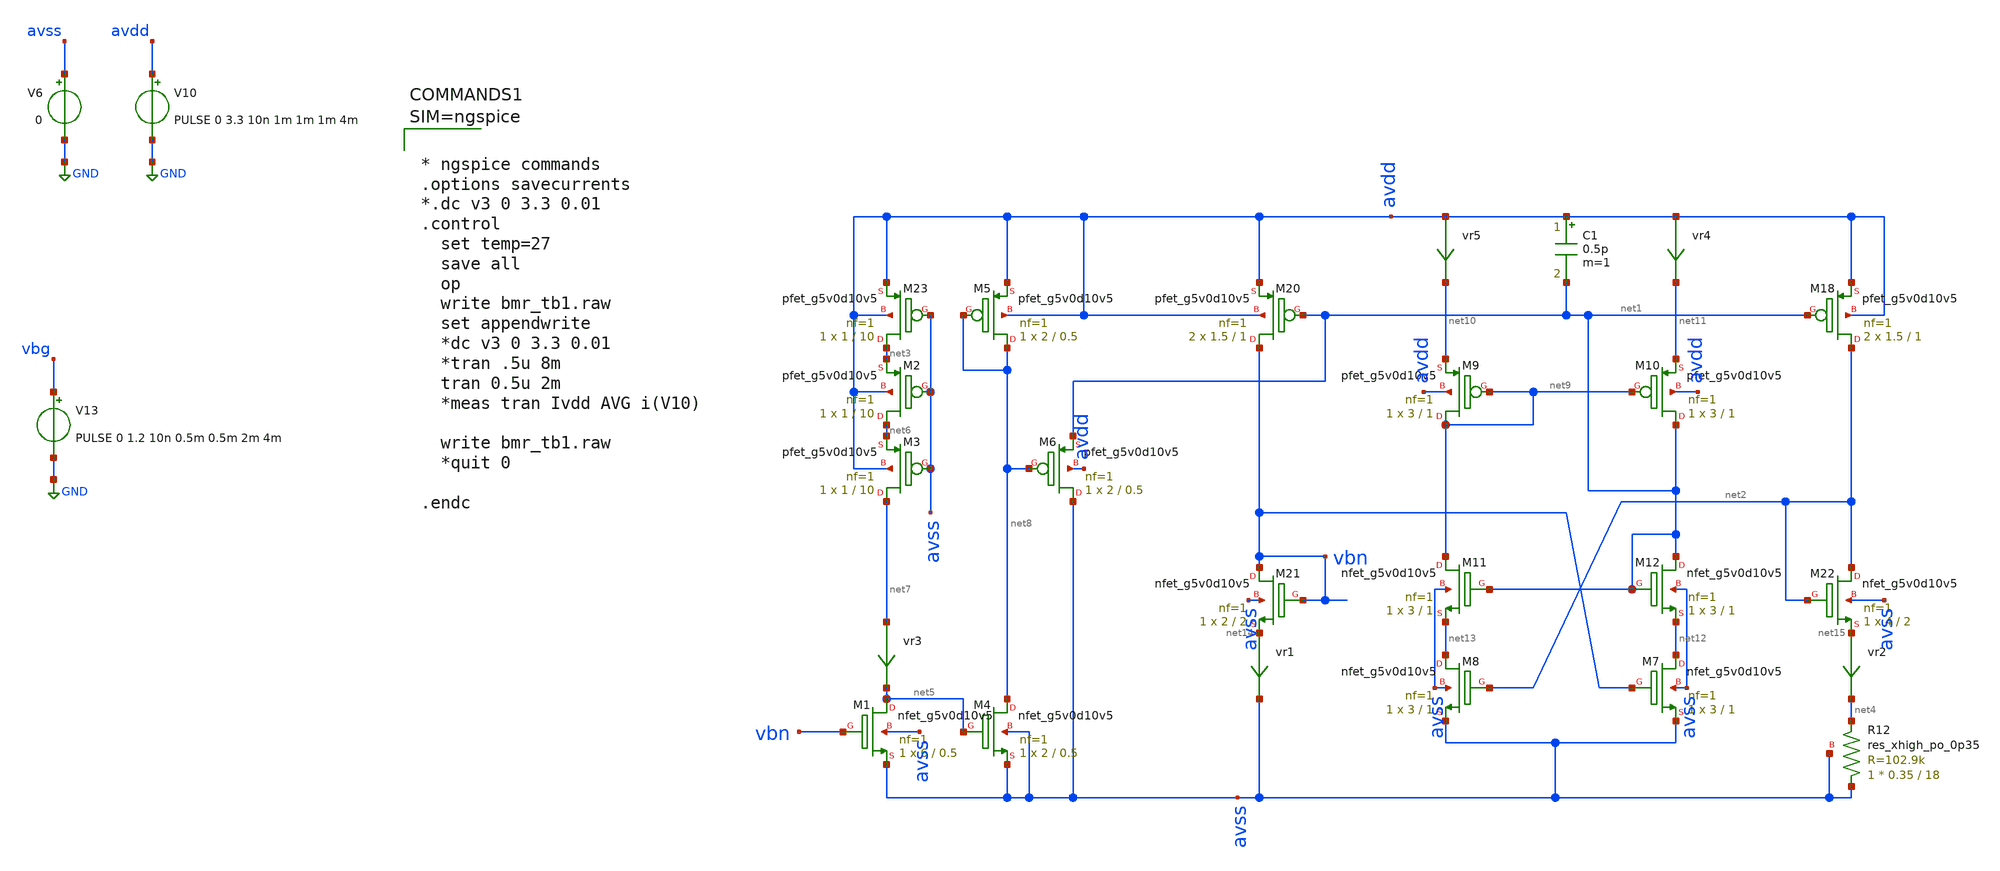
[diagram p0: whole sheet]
** sch_path: xschem_sim/bmr_tb1.sch
**.subckt bmr_tb1
XM18 net2 net1 avdd avdd sky130_fd_pr__pfet_g5v0d10v5 L=1 W=1.5 nf=1 ad='int((nf+1)/2) * W/nf * 0.29'
+ as='int((nf+2)/2) * W/nf * 0.29' pd='2*int((nf+1)/2) * (W/nf + 0.29)' ps='2*int((nf+2)/2) * (W/nf + 0.29)'
+ nrd='0.29 / W' nrs='0.29 / W' sa=0 sb=0 sd=0 mult=2 m=2
XM20 vbn net1 avdd avdd sky130_fd_pr__pfet_g5v0d10v5 L=1 W=1.5 nf=1 ad='int((nf+1)/2) * W/nf * 0.29'
+ as='int((nf+2)/2) * W/nf * 0.29' pd='2*int((nf+1)/2) * (W/nf + 0.29)' ps='2*int((nf+2)/2) * (W/nf + 0.29)'
+ nrd='0.29 / W' nrs='0.29 / W' sa=0 sb=0 sd=0 mult=2 m=2
XM21 vbn vbn net14 avss sky130_fd_pr__nfet_g5v0d10v5 L=2 W=2 nf=1 ad='int((nf+1)/2) * W/nf * 0.29' as='int((nf+2)/2) * W/nf * 0.29'
+ pd='2*int((nf+1)/2) * (W/nf + 0.29)' ps='2*int((nf+2)/2) * (W/nf + 0.29)' nrd='0.29 / W' nrs='0.29 / W'
+ sa=0 sb=0 sd=0 mult=1 m=1
XM22 net2 net2 net15 avss sky130_fd_pr__nfet_g5v0d10v5 L=2 W=4 nf=1 ad='int((nf+1)/2) * W/nf * 0.29'
+ as='int((nf+2)/2) * W/nf * 0.29' pd='2*int((nf+1)/2) * (W/nf + 0.29)' ps='2*int((nf+2)/2) * (W/nf + 0.29)'
+ nrd='0.29 / W' nrs='0.29 / W' sa=0 sb=0 sd=0 mult=1 m=1
XR12 avss net4 avss sky130_fd_pr__res_xhigh_po_0p35 L=18 mult=1 m=1
XM23 net3 avss avdd avdd sky130_fd_pr__pfet_g5v0d10v5 L=10 W=1 nf=1 ad='int((nf+1)/2) * W/nf * 0.29'
+ as='int((nf+2)/2) * W/nf * 0.29' pd='2*int((nf+1)/2) * (W/nf + 0.29)' ps='2*int((nf+2)/2) * (W/nf + 0.29)'
+ nrd='0.29 / W' nrs='0.29 / W' sa=0 sb=0 sd=0 mult=1 m=1
XM1 net5 vbn avss avss sky130_fd_pr__nfet_g5v0d10v5 L=0.5 W=6 nf=1 ad='int((nf+1)/2) * W/nf * 0.29' as='int((nf+2)/2) * W/nf * 0.29'
+ pd='2*int((nf+1)/2) * (W/nf + 0.29)' ps='2*int((nf+2)/2) * (W/nf + 0.29)' nrd='0.29 / W' nrs='0.29 / W'
+ sa=0 sb=0 sd=0 mult=1 m=1
vr1 net14 avss 0
.save i(vr1)
vr2 net15 net4 0
.save i(vr2)
vr3 net7 net5 0
.save i(vr3)
V10 avdd GND PULSE 0 3.3 10n 1m 1m 1m 4m
V6 avss GND 0
XM2 net6 avss net3 avdd sky130_fd_pr__pfet_g5v0d10v5 L=10 W=1 nf=1 ad='int((nf+1)/2) * W/nf * 0.29' as='int((nf+2)/2) * W/nf * 0.29'
+ pd='2*int((nf+1)/2) * (W/nf + 0.29)' ps='2*int((nf+2)/2) * (W/nf + 0.29)' nrd='0.29 / W' nrs='0.29 / W'
+ sa=0 sb=0 sd=0 mult=1 m=1
XM3 net7 avss net6 avdd sky130_fd_pr__pfet_g5v0d10v5 L=10 W=1 nf=1 ad='int((nf+1)/2) * W/nf * 0.29' as='int((nf+2)/2) * W/nf * 0.29'
+ pd='2*int((nf+1)/2) * (W/nf + 0.29)' ps='2*int((nf+2)/2) * (W/nf + 0.29)' nrd='0.29 / W' nrs='0.29 / W'
+ sa=0 sb=0 sd=0 mult=1 m=1
XM4 net8 net5 avss avss sky130_fd_pr__nfet_g5v0d10v5 L=0.5 W=2 nf=1 ad='int((nf+1)/2) * W/nf * 0.29'
+ as='int((nf+2)/2) * W/nf * 0.29' pd='2*int((nf+1)/2) * (W/nf + 0.29)' ps='2*int((nf+2)/2) * (W/nf + 0.29)'
+ nrd='0.29 / W' nrs='0.29 / W' sa=0 sb=0 sd=0 mult=1 m=1
XM5 net8 net8 avdd avdd sky130_fd_pr__pfet_g5v0d10v5 L=0.5 W=2 nf=1 ad='int((nf+1)/2) * W/nf * 0.29'
+ as='int((nf+2)/2) * W/nf * 0.29' pd='2*int((nf+1)/2) * (W/nf + 0.29)' ps='2*int((nf+2)/2) * (W/nf + 0.29)'
+ nrd='0.29 / W' nrs='0.29 / W' sa=0 sb=0 sd=0 mult=1 m=1
XM6 avss net8 net1 avdd sky130_fd_pr__pfet_g5v0d10v5 L=0.5 W=2 nf=1 ad='int((nf+1)/2) * W/nf * 0.29'
+ as='int((nf+2)/2) * W/nf * 0.29' pd='2*int((nf+1)/2) * (W/nf + 0.29)' ps='2*int((nf+2)/2) * (W/nf + 0.29)'
+ nrd='0.29 / W' nrs='0.29 / W' sa=0 sb=0 sd=0 mult=1 m=1
V13 vbg GND PULSE 0 1.2 10n 0.5m 0.5m 2m 4m
XM8 net13 net2 avss avss sky130_fd_pr__nfet_g5v0d10v5 L=1 W=3 nf=1 ad='int((nf+1)/2) * W/nf * 0.29' as='int((nf+2)/2) * W/nf * 0.29'
+ pd='2*int((nf+1)/2) * (W/nf + 0.29)' ps='2*int((nf+2)/2) * (W/nf + 0.29)' nrd='0.29 / W' nrs='0.29 / W'
+ sa=0 sb=0 sd=0 mult=1 m=1
XM7 net12 vbn avss avss sky130_fd_pr__nfet_g5v0d10v5 L=1 W=3 nf=1 ad='int((nf+1)/2) * W/nf * 0.29' as='int((nf+2)/2) * W/nf * 0.29'
+ pd='2*int((nf+1)/2) * (W/nf + 0.29)' ps='2*int((nf+2)/2) * (W/nf + 0.29)' nrd='0.29 / W' nrs='0.29 / W'
+ sa=0 sb=0 sd=0 mult=1 m=1
XM9 net9 net9 net10 avdd sky130_fd_pr__pfet_g5v0d10v5 L=1 W=3 nf=1 ad='int((nf+1)/2) * W/nf * 0.29' as='int((nf+2)/2) * W/nf * 0.29'
+ pd='2*int((nf+1)/2) * (W/nf + 0.29)' ps='2*int((nf+2)/2) * (W/nf + 0.29)' nrd='0.29 / W' nrs='0.29 / W'
+ sa=0 sb=0 sd=0 mult=1 m=1
XM10 net1 net9 net11 avdd sky130_fd_pr__pfet_g5v0d10v5 L=1 W=3 nf=1 ad='int((nf+1)/2) * W/nf * 0.29'
+ as='int((nf+2)/2) * W/nf * 0.29' pd='2*int((nf+1)/2) * (W/nf + 0.29)' ps='2*int((nf+2)/2) * (W/nf + 0.29)'
+ nrd='0.29 / W' nrs='0.29 / W' sa=0 sb=0 sd=0 mult=1 m=1
vr4 avdd net11 0
.save i(vr4)
vr5 avdd net10 0
.save i(vr5)
C1 avdd net1 0.5p m=1
XM11 net9 net1 net13 avss sky130_fd_pr__nfet_g5v0d10v5 L=1 W=3 nf=1 ad='int((nf+1)/2) * W/nf * 0.29'
+ as='int((nf+2)/2) * W/nf * 0.29' pd='2*int((nf+1)/2) * (W/nf + 0.29)' ps='2*int((nf+2)/2) * (W/nf + 0.29)'
+ nrd='0.29 / W' nrs='0.29 / W' sa=0 sb=0 sd=0 mult=1 m=1
XM12 net1 net1 net12 avss sky130_fd_pr__nfet_g5v0d10v5 L=1 W=3 nf=1 ad='int((nf+1)/2) * W/nf * 0.29'
+ as='int((nf+2)/2) * W/nf * 0.29' pd='2*int((nf+1)/2) * (W/nf + 0.29)' ps='2*int((nf+2)/2) * (W/nf + 0.29)'
+ nrd='0.29 / W' nrs='0.29 / W' sa=0 sb=0 sd=0 mult=1 m=1
**** begin user architecture code



* ngspice commands
.options savecurrents
*.dc v3 0 3.3 0.01
.control
  set temp=27
  save all
  op
  write bmr_tb1.raw
  set appendwrite
  *dc v3 0 3.3 0.01
  *tran .5u 8m
  tran 0.5u 2m
  *meas tran Ivdd AVG i(V10)

  write bmr_tb1.raw
  *quit 0

.endc



 .lib $::SKYWATER_MODELS/sky130.lib.spice tt

.include $::SKYWATER_STDCELLS/sky130_fd_sc_hd.spice
.include $::SKYWATER_STDCELLS/../../sky130_fd_sc_hvl/spice/sky130_fd_sc_hvl.spice


**** end user architecture code
**.ends
.GLOBAL GND
.end
